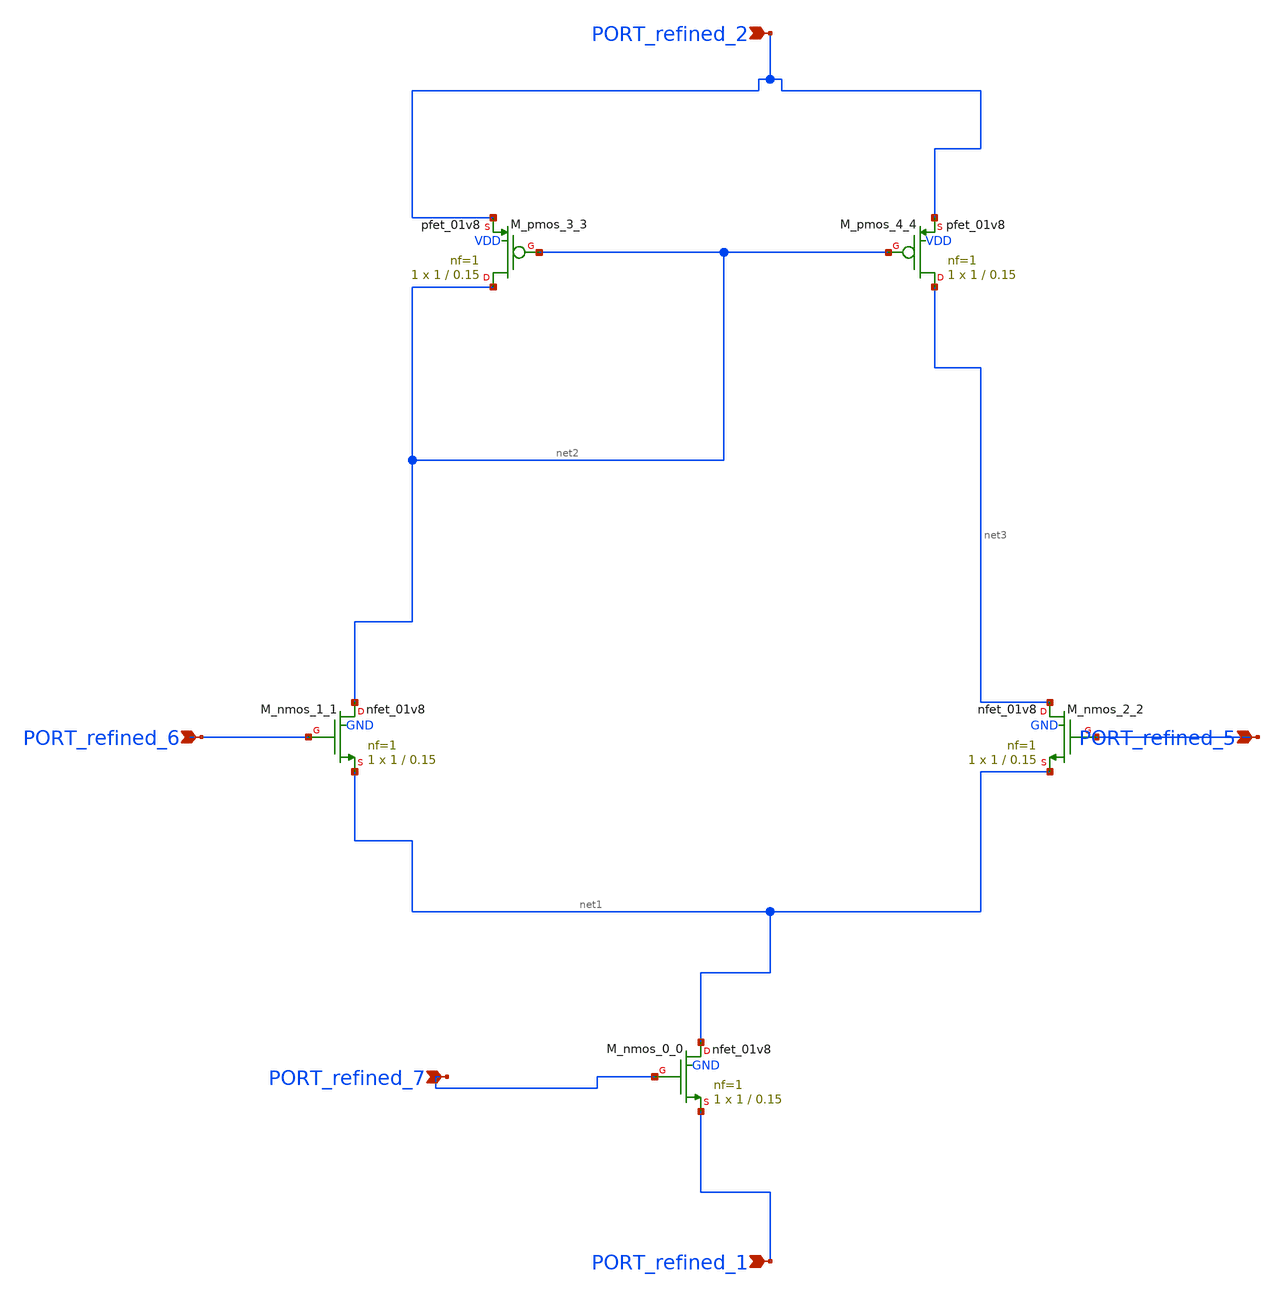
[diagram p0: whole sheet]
** sch_path: schematics/p04_fig5a_differential_amplifier.sch
**.subckt p04_fig5a_differential_amplifier PORT_refined_5 PORT_refined_2 PORT_refined_6
*+ PORT_refined_7 PORT_refined_1
*.ipin PORT_refined_5
*.ipin PORT_refined_2
*.ipin PORT_refined_6
*.ipin PORT_refined_7
*.ipin PORT_refined_1
XM_nmos_0_0 net1 PORT_refined_7 PORT_refined_1 GND sky130_fd_pr__nfet_01v8 L=0.15 W=1 nf=1 ad='int((1 + 1)/2) * 1 / 1 * 0.29'
+ as='int((1 + 2)/2) * 1 / 1 * 0.29' pd='2*int((1 + 1)/2) * (1 / 1 + 0.29)' ps='2*int((1 + 2)/2) * (1 / 1 + 0.29)'
+ nrd='0.29 / 1 ' nrs='0.29 / 1 ' sa=0 sb=0 sd=0 mult=1 m=1
XM_nmos_1_1 net2 PORT_refined_6 net1 GND sky130_fd_pr__nfet_01v8 L=0.15 W=1 nf=1 ad='int((1 + 1)/2) * 1 / 1 * 0.29'
+ as='int((1 + 2)/2) * 1 / 1 * 0.29' pd='2*int((1 + 1)/2) * (1 / 1 + 0.29)' ps='2*int((1 + 2)/2) * (1 / 1 + 0.29)'
+ nrd='0.29 / 1 ' nrs='0.29 / 1 ' sa=0 sb=0 sd=0 mult=1 m=1
XM_nmos_2_2 net3 PORT_refined_5 net1 GND sky130_fd_pr__nfet_01v8 L=0.15 W=1 nf=1 ad='int((1 + 1)/2) * 1 / 1 * 0.29'
+ as='int((1 + 2)/2) * 1 / 1 * 0.29' pd='2*int((1 + 1)/2) * (1 / 1 + 0.29)' ps='2*int((1 + 2)/2) * (1 / 1 + 0.29)'
+ nrd='0.29 / 1 ' nrs='0.29 / 1 ' sa=0 sb=0 sd=0 mult=1 m=1
XM_pmos_3_3 net2 net2 PORT_refined_2 VDD sky130_fd_pr__pfet_01v8 L=0.15 W=1 nf=1 ad='int((1 + 1)/2) * 1 / 1 * 0.29'
+ as='int((1 + 2)/2) * 1 / 1 * 0.29' pd='2*int((1 + 1)/2) * (1 / 1 + 0.29)' ps='2*int((1 + 2)/2) * (1 / 1 + 0.29)'
+ nrd='0.29 / 1 ' nrs='0.29 / 1 ' sa=0 sb=0 sd=0 mult=1 m=1
XM_pmos_4_4 net3 net2 PORT_refined_2 VDD sky130_fd_pr__pfet_01v8 L=0.15 W=1 nf=1 ad='int((1 + 1)/2) * 1 / 1 * 0.29'
+ as='int((1 + 2)/2) * 1 / 1 * 0.29' pd='2*int((1 + 1)/2) * (1 / 1 + 0.29)' ps='2*int((1 + 2)/2) * (1 / 1 + 0.29)'
+ nrd='0.29 / 1 ' nrs='0.29 / 1 ' sa=0 sb=0 sd=0 mult=1 m=1
**.ends
.end
